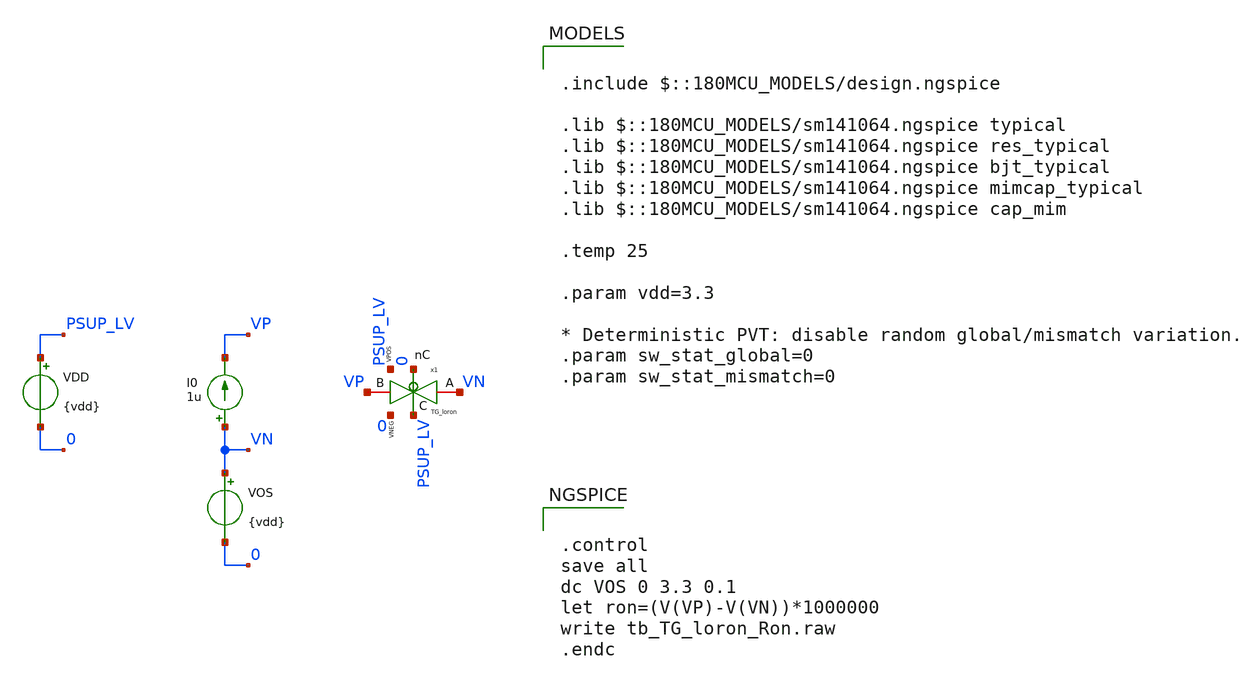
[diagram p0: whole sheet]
** sch_path: xschem/blocks/TG_loron/tb_TG_loron_Ron.sch
**.subckt tb_TG_loron_Ron
VDD PSUP_LV 0 {vdd}
I0 VN VP 1u
VOS VN 0 {vdd}
x1 PSUP_LV VN VP 0 PSUP_LV 0 TG_loron
**** begin user architecture code

.include $::180MCU_MODELS/design.ngspice

.lib $::180MCU_MODELS/sm141064.ngspice typical
.lib $::180MCU_MODELS/sm141064.ngspice res_typical
.lib $::180MCU_MODELS/sm141064.ngspice bjt_typical
.lib $::180MCU_MODELS/sm141064.ngspice mimcap_typical
.lib $::180MCU_MODELS/sm141064.ngspice cap_mim

.temp 25

.param vdd=3.3

* Deterministic PVT: disable random global/mismatch variation.
.param sw_stat_global=0
.param sw_stat_mismatch=0



.control
save all
dc VOS 0 3.3 0.1
let ron=(V(VP)-V(VN))*1000000
write tb_TG_loron_Ron.raw
.endc


**** end user architecture code
**.ends

* expanding   symbol:  blocks/TG_loron/TG_loron.sym # of pins=6
** sym_path: xschem/blocks/TG_loron/TG_loron.sym
** sch_path: xschem/blocks/TG_loron/TG_loron.sch
.subckt TG_loron C A B nC VPOS VNEG
*.iopin A
*.iopin B
*.ipin C
*.ipin nC
*.ipin VPOS
*.ipin VNEG
XM3 A C B VNEG nfet_03v3 L=2u W=10u nf=1 ad='int((nf+1)/2) * W/nf * 0.18u' as='int((nf+2)/2) * W/nf * 0.18u'
+ pd='2*int((nf+1)/2) * (W/nf + 0.18u)' ps='2*int((nf+2)/2) * (W/nf + 0.18u)' nrd='0.18u / W' nrs='0.18u / W'
+ sa=0 sb=0 sd=0 m=8
XM4 A nC B VPOS pfet_03v3 L=2u W=10u nf=1 ad='int((nf+1)/2) * W/nf * 0.18u' as='int((nf+2)/2) * W/nf * 0.18u'
+ pd='2*int((nf+1)/2) * (W/nf + 0.18u)' ps='2*int((nf+2)/2) * (W/nf + 0.18u)' nrd='0.18u / W' nrs='0.18u / W'
+ sa=0 sb=0 sd=0 m=16
.ends

.end
